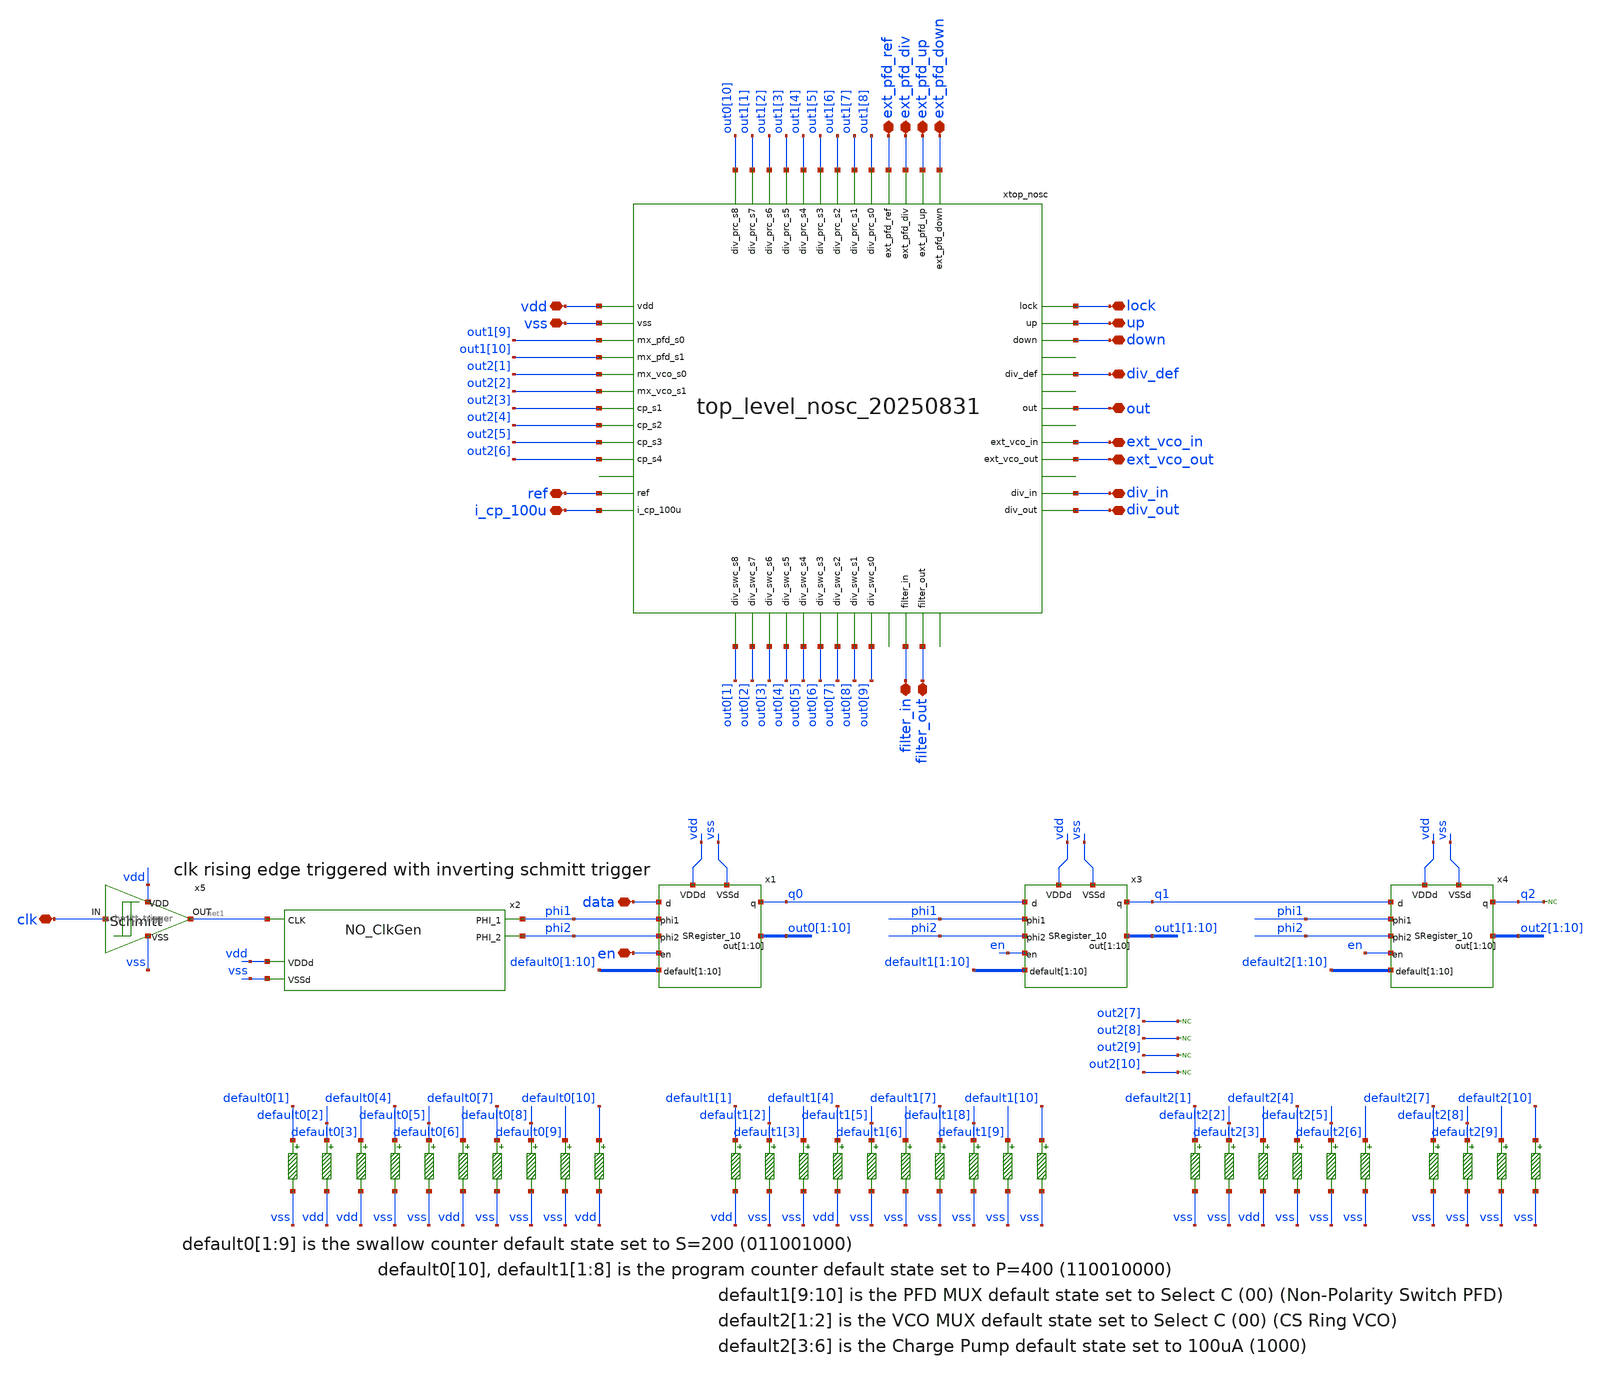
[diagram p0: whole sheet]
** sch_path: designs/libs/top_level/top_level_20250831/top_level_sc_20250831/top_level_sc_20250831.sch
**.subckt top_level_sc_20250831 vdd vss ref i_cp_100u filter_in filter_out ext_pfd_ref ext_pfd_up
*+ ext_pfd_down ext_pfd_div up down out lock ext_vco_out ext_vco_in div_out div_in div_def clk data en
*.iopin vdd
*.iopin vss
*.iopin ref
*.iopin i_cp_100u
*.iopin filter_in
*.iopin filter_out
*.iopin ext_pfd_ref
*.iopin ext_pfd_up
*.iopin ext_pfd_down
*.iopin ext_pfd_div
*.iopin up
*.iopin down
*.iopin out
*.iopin lock
*.iopin ext_vco_out
*.iopin ext_vco_in
*.iopin div_out
*.iopin div_in
*.iopin div_def
*.iopin clk
*.iopin data
*.iopin en
xtop_nosc vdd vss out1[9] out1[10] out2[1] out2[2] out0[1] out2[3] out2[4] out2[5] out2[6] out0[2]
+ out0[3] out0[4] out0[5] out0[6] out0[7] out0[8] out0[9] out0[10] out1[1] out1[2] out1[3] out1[4] out1[5]
+ out1[6] out1[7] out1[8] ref i_cp_100u ext_pfd_ref ext_pfd_div ext_pfd_up ext_pfd_down lock up down
+ filter_out ext_vco_in div_in div_out out filter_in ext_vco_out div_def top_level_nosc_20250831
x2 phi2 net1 phi1 vdd vss NO_ClkGen
x1 vdd vss phi1 phi2 en default0[1] default0[2] default0[3] default0[4] default0[5] default0[6]
+ default0[7] default0[8] default0[9] default0[10] data q0 out0[1] out0[2] out0[3] out0[4] out0[5] out0[6]
+ out0[7] out0[8] out0[9] out0[10] SRegister_10
x3 vdd vss phi1 phi2 en default1[1] default1[2] default1[3] default1[4] default1[5] default1[6]
+ default1[7] default1[8] default1[9] default1[10] q0 q1 out1[1] out1[2] out1[3] out1[4] out1[5] out1[6] out1[7]
+ out1[8] out1[9] out1[10] SRegister_10
x4 vdd vss phi1 phi2 en default2[1] default2[2] default2[3] default2[4] default2[5] default2[6]
+ default2[7] default2[8] default2[9] default2[10] q1 q2 out2[1] out2[2] out2[3] out2[4] out2[5] out2[6] out2[7]
+ out2[8] out2[9] out2[10] SRegister_10
* noconn q2
x5 clk net1 vdd vss schmitt_trigger
* noconn out2[7]
* noconn out2[8]
* noconn out2[9]
* noconn out2[10]
R1 default1[1] vdd 0.01 m=1
R2 default1[2] vss 0.01 m=1
R3 default1[3] vss 0.01 m=1
R4 default1[4] vdd 0.01 m=1
R5 default1[5] vss 0.01 m=1
R6 default1[6] vss 0.01 m=1
R7 default1[7] vss 0.01 m=1
R8 default1[8] vss 0.01 m=1
R9 default1[9] vss 0.01 m=1
R10 default1[10] vss 0.01 m=1
R11 default2[1] vss 0.01 m=1
R12 default2[2] vss 0.01 m=1
R13 default2[3] vdd 0.01 m=1
R14 default2[4] vss 0.01 m=1
R15 default2[5] vss 0.01 m=1
R16 default2[6] vss 0.01 m=1
R17 default2[7] vss 0.01 m=1
R18 default2[8] vss 0.01 m=1
R19 default2[9] vss 0.01 m=1
R20 default2[10] vss 0.01 m=1
R21 default0[1] vss 0.01 m=1
R22 default0[2] vdd 0.01 m=1
R23 default0[3] vdd 0.01 m=1
R24 default0[4] vss 0.01 m=1
R25 default0[5] vss 0.01 m=1
R26 default0[6] vdd 0.01 m=1
R27 default0[7] vss 0.01 m=1
R28 default0[8] vss 0.01 m=1
R29 default0[9] vss 0.01 m=1
R30 default0[10] vdd 0.01 m=1
**.ends
.end
